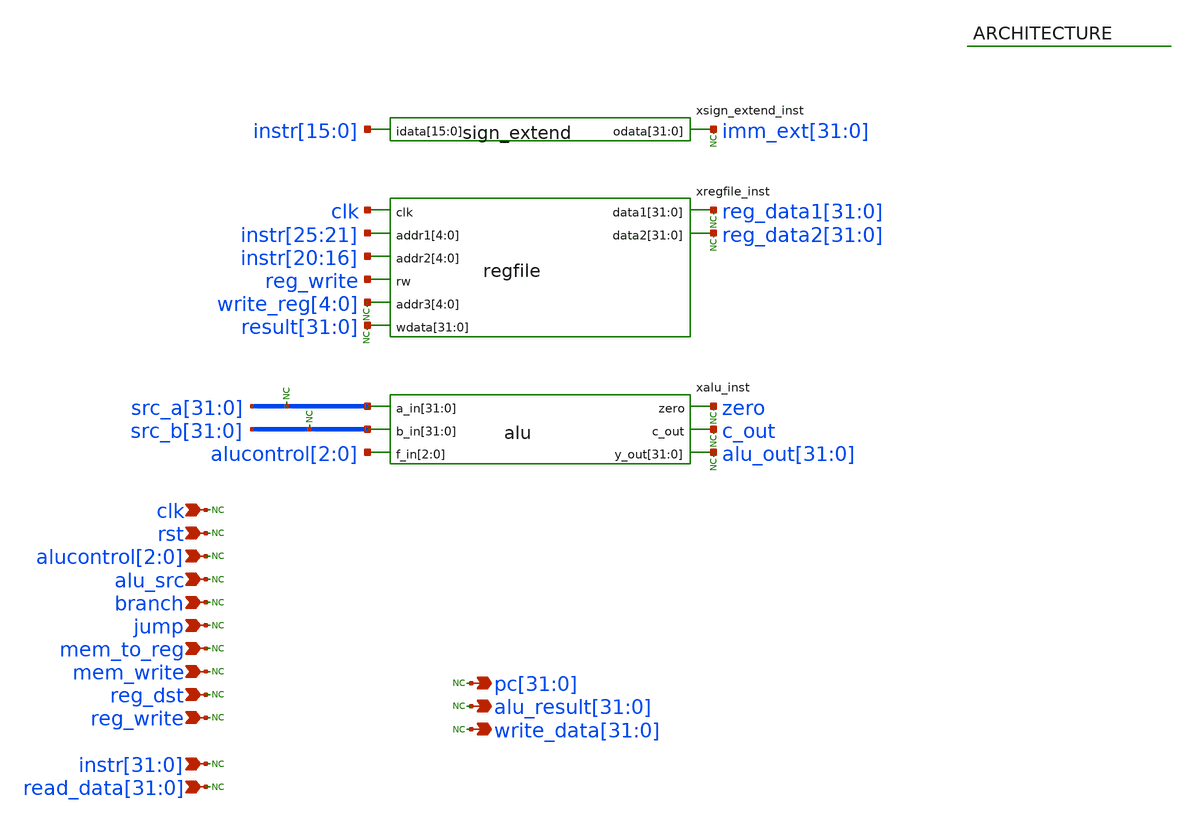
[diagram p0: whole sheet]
** sch_path: mips_cpu/datapath.sch
* Licensed under the Apache License, Version 2.0 (the "License");
* you may not use this file except in compliance with the License.
* You may obtain a copy of the License at
* https://www.apache.org/licenses/LICENSE-2.0
* Unless required by applicable law or agreed to in writing, software
* distributed under the License is distributed on an "AS IS" BASIS,
* WITHOUT WARRANTIES OR CONDITIONS OF ANY KIND, either express or implied.
* See the License for the specific language governing permissions and
* limitations under the License.
**.subckt datapath clk rst alucontrol[2],alucontrol[1],alucontrol[0] alu_src branch jump mem_to_reg
*+ reg_dst reg_write
*+ instr[31],instr[30],instr[29],instr[28],instr[27],instr[26],instr[25],instr[24],instr[23],instr[22],instr[21],instr[20],instr[19],instr[18],instr[17],instr[16],instr[15],instr[14],instr[13],instr[12],instr[11],instr[10],instr[9],instr[8],instr[7],instr[6],instr[5],instr[4],instr[3],instr[2],instr[1],instr[0]
*+ pc[31],pc[30],pc[29],pc[28],pc[27],pc[26],pc[25],pc[24],pc[23],pc[22],pc[21],pc[20],pc[19],pc[18],pc[17],pc[16],pc[15],pc[14],pc[13],pc[12],pc[11],pc[10],pc[9],pc[8],pc[7],pc[6],pc[5],pc[4],pc[3],pc[2],pc[1],pc[0]
*+ read_data[31],read_data[30],read_data[29],read_data[28],read_data[27],read_data[26],read_data[25],read_data[24],read_data[23],read_data[22],read_data[21],read_data[20],read_data[19],read_data[18],read_data[17],read_data[16],read_data[15],read_data[14],read_data[13],read_data[12],read_data[11],read_data[10],read_data[9],read_data[8],read_data[7],read_data[6],read_data[5],read_data[4],read_data[3],read_data[2],read_data[1],read_data[0]
*+ alu_result[31],alu_result[30],alu_result[29],alu_result[28],alu_result[27],alu_result[26],alu_result[25],alu_result[24],alu_result[23],alu_result[22],alu_result[21],alu_result[20],alu_result[19],alu_result[18],alu_result[17],alu_result[16],alu_result[15],alu_result[14],alu_result[13],alu_result[12],alu_result[11],alu_result[10],alu_result[9],alu_result[8],alu_result[7],alu_result[6],alu_result[5],alu_result[4],alu_result[3],alu_result[2],alu_result[1],alu_result[0]
*+ write_data[31],write_data[30],write_data[29],write_data[28],write_data[27],write_data[26],write_data[25],write_data[24],write_data[23],write_data[22],write_data[21],write_data[20],write_data[19],write_data[18],write_data[17],write_data[16],write_data[15],write_data[14],write_data[13],write_data[12],write_data[11],write_data[10],write_data[9],write_data[8],write_data[7],write_data[6],write_data[5],write_data[4],write_data[3],write_data[2],write_data[1],write_data[0] mem_write
*.ipin clk
*.ipin rst
*.ipin alucontrol[2],alucontrol[1],alucontrol[0]
*.ipin alu_src
*.ipin branch
*.ipin jump
*.ipin mem_to_reg
*.ipin reg_dst
*.ipin reg_write
*.ipin
*+ instr[31],instr[30],instr[29],instr[28],instr[27],instr[26],instr[25],instr[24],instr[23],instr[22],instr[21],instr[20],instr[19],instr[18],instr[17],instr[16],instr[15],instr[14],instr[13],instr[12],instr[11],instr[10],instr[9],instr[8],instr[7],instr[6],instr[5],instr[4],instr[3],instr[2],instr[1],instr[0]
*.opin
*+ pc[31],pc[30],pc[29],pc[28],pc[27],pc[26],pc[25],pc[24],pc[23],pc[22],pc[21],pc[20],pc[19],pc[18],pc[17],pc[16],pc[15],pc[14],pc[13],pc[12],pc[11],pc[10],pc[9],pc[8],pc[7],pc[6],pc[5],pc[4],pc[3],pc[2],pc[1],pc[0]
*.ipin
*+ read_data[31],read_data[30],read_data[29],read_data[28],read_data[27],read_data[26],read_data[25],read_data[24],read_data[23],read_data[22],read_data[21],read_data[20],read_data[19],read_data[18],read_data[17],read_data[16],read_data[15],read_data[14],read_data[13],read_data[12],read_data[11],read_data[10],read_data[9],read_data[8],read_data[7],read_data[6],read_data[5],read_data[4],read_data[3],read_data[2],read_data[1],read_data[0]
*.opin
*+ alu_result[31],alu_result[30],alu_result[29],alu_result[28],alu_result[27],alu_result[26],alu_result[25],alu_result[24],alu_result[23],alu_result[22],alu_result[21],alu_result[20],alu_result[19],alu_result[18],alu_result[17],alu_result[16],alu_result[15],alu_result[14],alu_result[13],alu_result[12],alu_result[11],alu_result[10],alu_result[9],alu_result[8],alu_result[7],alu_result[6],alu_result[5],alu_result[4],alu_result[3],alu_result[2],alu_result[1],alu_result[0]
*.opin
*+ write_data[31],write_data[30],write_data[29],write_data[28],write_data[27],write_data[26],write_data[25],write_data[24],write_data[23],write_data[22],write_data[21],write_data[20],write_data[19],write_data[18],write_data[17],write_data[16],write_data[15],write_data[14],write_data[13],write_data[12],write_data[11],write_data[10],write_data[9],write_data[8],write_data[7],write_data[6],write_data[5],write_data[4],write_data[3],write_data[2],write_data[1],write_data[0]
*.ipin mem_write
xregfile_inst clk instr[25] instr[24] instr[23] instr[22] instr[21] instr[20] instr[19] instr[18]
+ instr[17] instr[16] reg_data1[31] reg_data1[30] reg_data1[29] reg_data1[28] reg_data1[27] reg_data1[26]
+ reg_data1[25] reg_data1[24] reg_data1[23] reg_data1[22] reg_data1[21] reg_data1[20] reg_data1[19] reg_data1[18]
+ reg_data1[17] reg_data1[16] reg_data1[15] reg_data1[14] reg_data1[13] reg_data1[12] reg_data1[11] reg_data1[10]
+ reg_data1[9] reg_data1[8] reg_data1[7] reg_data1[6] reg_data1[5] reg_data1[4] reg_data1[3] reg_data1[2]
+ reg_data1[1] reg_data1[0] reg_write reg_data2[31] reg_data2[30] reg_data2[29] reg_data2[28] reg_data2[27]
+ reg_data2[26] reg_data2[25] reg_data2[24] reg_data2[23] reg_data2[22] reg_data2[21] reg_data2[20] reg_data2[19]
+ reg_data2[18] reg_data2[17] reg_data2[16] reg_data2[15] reg_data2[14] reg_data2[13] reg_data2[12] reg_data2[11]
+ reg_data2[10] reg_data2[9] reg_data2[8] reg_data2[7] reg_data2[6] reg_data2[5] reg_data2[4] reg_data2[3]
+ reg_data2[2] reg_data2[1] reg_data2[0] write_reg[4] write_reg[3] write_reg[2] write_reg[1] write_reg[0]
+ result[31] result[30] result[29] result[28] result[27] result[26] result[25] result[24] result[23] result[22]
+ result[21] result[20] result[19] result[18] result[17] result[16] result[15] result[14] result[13] result[12]
+ result[11] result[10] result[9] result[8] result[7] result[6] result[5] result[4] result[3] result[2]
+ result[1] result[0] regfile
xalu_inst src_a[31] src_a[30] src_a[29] src_a[28] src_a[27] src_a[26] src_a[25] src_a[24] src_a[23]
+ src_a[22] src_a[21] src_a[20] src_a[19] src_a[18] src_a[17] src_a[16] src_a[15] src_a[14] src_a[13] src_a[12]
+ src_a[11] src_a[10] src_a[9] src_a[8] src_a[7] src_a[6] src_a[5] src_a[4] src_a[3] src_a[2] src_a[1] src_a[0]
+ zero src_b[31] src_b[30] src_b[29] src_b[28] src_b[27] src_b[26] src_b[25] src_b[24] src_b[23] src_b[22]
+ src_b[21] src_b[20] src_b[19] src_b[18] src_b[17] src_b[16] src_b[15] src_b[14] src_b[13] src_b[12] src_b[11]
+ src_b[10] src_b[9] src_b[8] src_b[7] src_b[6] src_b[5] src_b[4] src_b[3] src_b[2] src_b[1] src_b[0] c_out
+ alu_out[31] alu_out[30] alu_out[29] alu_out[28] alu_out[27] alu_out[26] alu_out[25] alu_out[24] alu_out[23]
+ alu_out[22] alu_out[21] alu_out[20] alu_out[19] alu_out[18] alu_out[17] alu_out[16] alu_out[15] alu_out[14]
+ alu_out[13] alu_out[12] alu_out[11] alu_out[10] alu_out[9] alu_out[8] alu_out[7] alu_out[6] alu_out[5]
+ alu_out[4] alu_out[3] alu_out[2] alu_out[1] alu_out[0] alucontrol[2] alucontrol[1] alucontrol[0] alu
xsign_extend_inst instr[15] instr[14] instr[13] instr[12] instr[11] instr[10] instr[9] instr[8]
+ instr[7] instr[6] instr[5] instr[4] instr[3] instr[2] instr[1] instr[0] imm_ext[31] imm_ext[30] imm_ext[29]
+ imm_ext[28] imm_ext[27] imm_ext[26] imm_ext[25] imm_ext[24] imm_ext[23] imm_ext[22] imm_ext[21] imm_ext[20]
+ imm_ext[19] imm_ext[18] imm_ext[17] imm_ext[16] imm_ext[15] imm_ext[14] imm_ext[13] imm_ext[12] imm_ext[11]
+ imm_ext[10] imm_ext[9] imm_ext[8] imm_ext[7] imm_ext[6] imm_ext[5] imm_ext[4] imm_ext[3] imm_ext[2] imm_ext[1]
+ imm_ext[0] sign_extend
* noconn clk
* noconn rst
* noconn alucontrol[2:0]
* noconn alu_src
* noconn branch
* noconn jump
* noconn mem_to_reg
* noconn mem_write
* noconn reg_dst
* noconn reg_write
* noconn instr[31:0]
* noconn read_data[31:0]
* noconn pc[31:0]
* noconn write_data[31:0]
* noconn alu_result[31:0]
* noconn alu_out[31:0]
* noconn src_a[31:0]
* noconn src_b[31:0]
* noconn imm_ext[31:0]
* noconn reg_data1[31:0]
* noconn reg_data2[31:0]
* noconn result[31:0]
* noconn c_out
* noconn zero
* noconn write_reg[4:0]
**.ends

* expanding   symbol:  mips_cpu/regfile.sym # of pins=8
** sym_path: mips_cpu/regfile.sym
** sch_path: mips_cpu/regfile.sch
.subckt regfile clk addr1[4] addr1[3] addr1[2] addr1[1] addr1[0] addr2[4] addr2[3] addr2[2] addr2[1]
+ addr2[0] data1[31] data1[30] data1[29] data1[28] data1[27] data1[26] data1[25] data1[24] data1[23] data1[22]
+ data1[21] data1[20] data1[19] data1[18] data1[17] data1[16] data1[15] data1[14] data1[13] data1[12] data1[11]
+ data1[10] data1[9] data1[8] data1[7] data1[6] data1[5] data1[4] data1[3] data1[2] data1[1] data1[0] rw
+ data2[31] data2[30] data2[29] data2[28] data2[27] data2[26] data2[25] data2[24] data2[23] data2[22] data2[21]
+ data2[20] data2[19] data2[18] data2[17] data2[16] data2[15] data2[14] data2[13] data2[12] data2[11] data2[10]
+ data2[9] data2[8] data2[7] data2[6] data2[5] data2[4] data2[3] data2[2] data2[1] data2[0] addr3[4] addr3[3]
+ addr3[2] addr3[1] addr3[0] wdata[31] wdata[30] wdata[29] wdata[28] wdata[27] wdata[26] wdata[25] wdata[24]
+ wdata[23] wdata[22] wdata[21] wdata[20] wdata[19] wdata[18] wdata[17] wdata[16] wdata[15] wdata[14] wdata[13]
+ wdata[12] wdata[11] wdata[10] wdata[9] wdata[8] wdata[7] wdata[6] wdata[5] wdata[4] wdata[3] wdata[2]
+ wdata[1] wdata[0]
*.ipin clk
*.ipin addr1[4],addr1[3],addr1[2],addr1[1],addr1[0]
*.ipin addr2[4],addr2[3],addr2[2],addr2[1],addr2[0]
*.opin
*+ data1[31],data1[30],data1[29],data1[28],data1[27],data1[26],data1[25],data1[24],data1[23],data1[22],data1[21],data1[20],data1[19],data1[18],data1[17],data1[16],data1[15],data1[14],data1[13],data1[12],data1[11],data1[10],data1[9],data1[8],data1[7],data1[6],data1[5],data1[4],data1[3],data1[2],data1[1],data1[0]
*.opin
*+ data2[31],data2[30],data2[29],data2[28],data2[27],data2[26],data2[25],data2[24],data2[23],data2[22],data2[21],data2[20],data2[19],data2[18],data2[17],data2[16],data2[15],data2[14],data2[13],data2[12],data2[11],data2[10],data2[9],data2[8],data2[7],data2[6],data2[5],data2[4],data2[3],data2[2],data2[1],data2[0]
*.ipin rw
*.ipin addr3[4],addr3[3],addr3[2],addr3[1],addr3[0]
*.ipin
*+ wdata[31],wdata[30],wdata[29],wdata[28],wdata[27],wdata[26],wdata[25],wdata[24],wdata[23],wdata[22],wdata[21],wdata[20],wdata[19],wdata[18],wdata[17],wdata[16],wdata[15],wdata[14],wdata[13],wdata[12],wdata[11],wdata[10],wdata[9],wdata[8],wdata[7],wdata[6],wdata[5],wdata[4],wdata[3],wdata[2],wdata[1],wdata[0]
* noconn clk
* noconn addr1[4:0]
* noconn addr2[4:0]
* noconn rw
* noconn addr3[4:0]
* noconn wdata[31:0]
* noconn data1[31:0]
* noconn data2[31:0]
.ends


* expanding   symbol:  mips_cpu/alu.sym # of pins=6
** sym_path: mips_cpu/alu.sym
** sch_path: mips_cpu/alu.sch
.subckt alu a_in[31] a_in[30] a_in[29] a_in[28] a_in[27] a_in[26] a_in[25] a_in[24] a_in[23]
+ a_in[22] a_in[21] a_in[20] a_in[19] a_in[18] a_in[17] a_in[16] a_in[15] a_in[14] a_in[13] a_in[12] a_in[11]
+ a_in[10] a_in[9] a_in[8] a_in[7] a_in[6] a_in[5] a_in[4] a_in[3] a_in[2] a_in[1] a_in[0] zero b_in[31]
+ b_in[30] b_in[29] b_in[28] b_in[27] b_in[26] b_in[25] b_in[24] b_in[23] b_in[22] b_in[21] b_in[20] b_in[19]
+ b_in[18] b_in[17] b_in[16] b_in[15] b_in[14] b_in[13] b_in[12] b_in[11] b_in[10] b_in[9] b_in[8] b_in[7]
+ b_in[6] b_in[5] b_in[4] b_in[3] b_in[2] b_in[1] b_in[0] c_out y_out[31] y_out[30] y_out[29] y_out[28]
+ y_out[27] y_out[26] y_out[25] y_out[24] y_out[23] y_out[22] y_out[21] y_out[20] y_out[19] y_out[18] y_out[17]
+ y_out[16] y_out[15] y_out[14] y_out[13] y_out[12] y_out[11] y_out[10] y_out[9] y_out[8] y_out[7] y_out[6]
+ y_out[5] y_out[4] y_out[3] y_out[2] y_out[1] y_out[0] f_in[2] f_in[1] f_in[0]
*.ipin
*+ a_in[31],a_in[30],a_in[29],a_in[28],a_in[27],a_in[26],a_in[25],a_in[24],a_in[23],a_in[22],a_in[21],a_in[20],a_in[19],a_in[18],a_in[17],a_in[16],a_in[15],a_in[14],a_in[13],a_in[12],a_in[11],a_in[10],a_in[9],a_in[8],a_in[7],a_in[6],a_in[5],a_in[4],a_in[3],a_in[2],a_in[1],a_in[0]
*.opin zero
*.ipin
*+ b_in[31],b_in[30],b_in[29],b_in[28],b_in[27],b_in[26],b_in[25],b_in[24],b_in[23],b_in[22],b_in[21],b_in[20],b_in[19],b_in[18],b_in[17],b_in[16],b_in[15],b_in[14],b_in[13],b_in[12],b_in[11],b_in[10],b_in[9],b_in[8],b_in[7],b_in[6],b_in[5],b_in[4],b_in[3],b_in[2],b_in[1],b_in[0]
*.ipin f_in[2],f_in[1],f_in[0]
*.opin c_out
*.opin
*+ y_out[31],y_out[30],y_out[29],y_out[28],y_out[27],y_out[26],y_out[25],y_out[24],y_out[23],y_out[22],y_out[21],y_out[20],y_out[19],y_out[18],y_out[17],y_out[16],y_out[15],y_out[14],y_out[13],y_out[12],y_out[11],y_out[10],y_out[9],y_out[8],y_out[7],y_out[6],y_out[5],y_out[4],y_out[3],y_out[2],y_out[1],y_out[0]
* noconn zero
* noconn a_in[31:0]
* noconn b_in[31:0]
* noconn f_in[2:0]
* noconn c_out
* noconn y_out[31:0]
.ends


* expanding   symbol:  mips_cpu/sign_extend.sym # of pins=2
** sym_path: mips_cpu/sign_extend.sym
** sch_path: mips_cpu/sign_extend.sch
.subckt sign_extend idata[15] idata[14] idata[13] idata[12] idata[11] idata[10] idata[9] idata[8]
+ idata[7] idata[6] idata[5] idata[4] idata[3] idata[2] idata[1] idata[0] odata[31] odata[30] odata[29]
+ odata[28] odata[27] odata[26] odata[25] odata[24] odata[23] odata[22] odata[21] odata[20] odata[19] odata[18]
+ odata[17] odata[16] odata[15] odata[14] odata[13] odata[12] odata[11] odata[10] odata[9] odata[8] odata[7]
+ odata[6] odata[5] odata[4] odata[3] odata[2] odata[1] odata[0]
*.opin
*+ odata[31],odata[30],odata[29],odata[28],odata[27],odata[26],odata[25],odata[24],odata[23],odata[22],odata[21],odata[20],odata[19],odata[18],odata[17],odata[16],odata[15],odata[14],odata[13],odata[12],odata[11],odata[10],odata[9],odata[8],odata[7],odata[6],odata[5],odata[4],odata[3],odata[2],odata[1],odata[0]
*.ipin
*+ idata[15],idata[14],idata[13],idata[12],idata[11],idata[10],idata[9],idata[8],idata[7],idata[6],idata[5],idata[4],idata[3],idata[2],idata[1],idata[0]
* noconn odata[31:0]
* noconn idata[15:0]
.ends

.end
